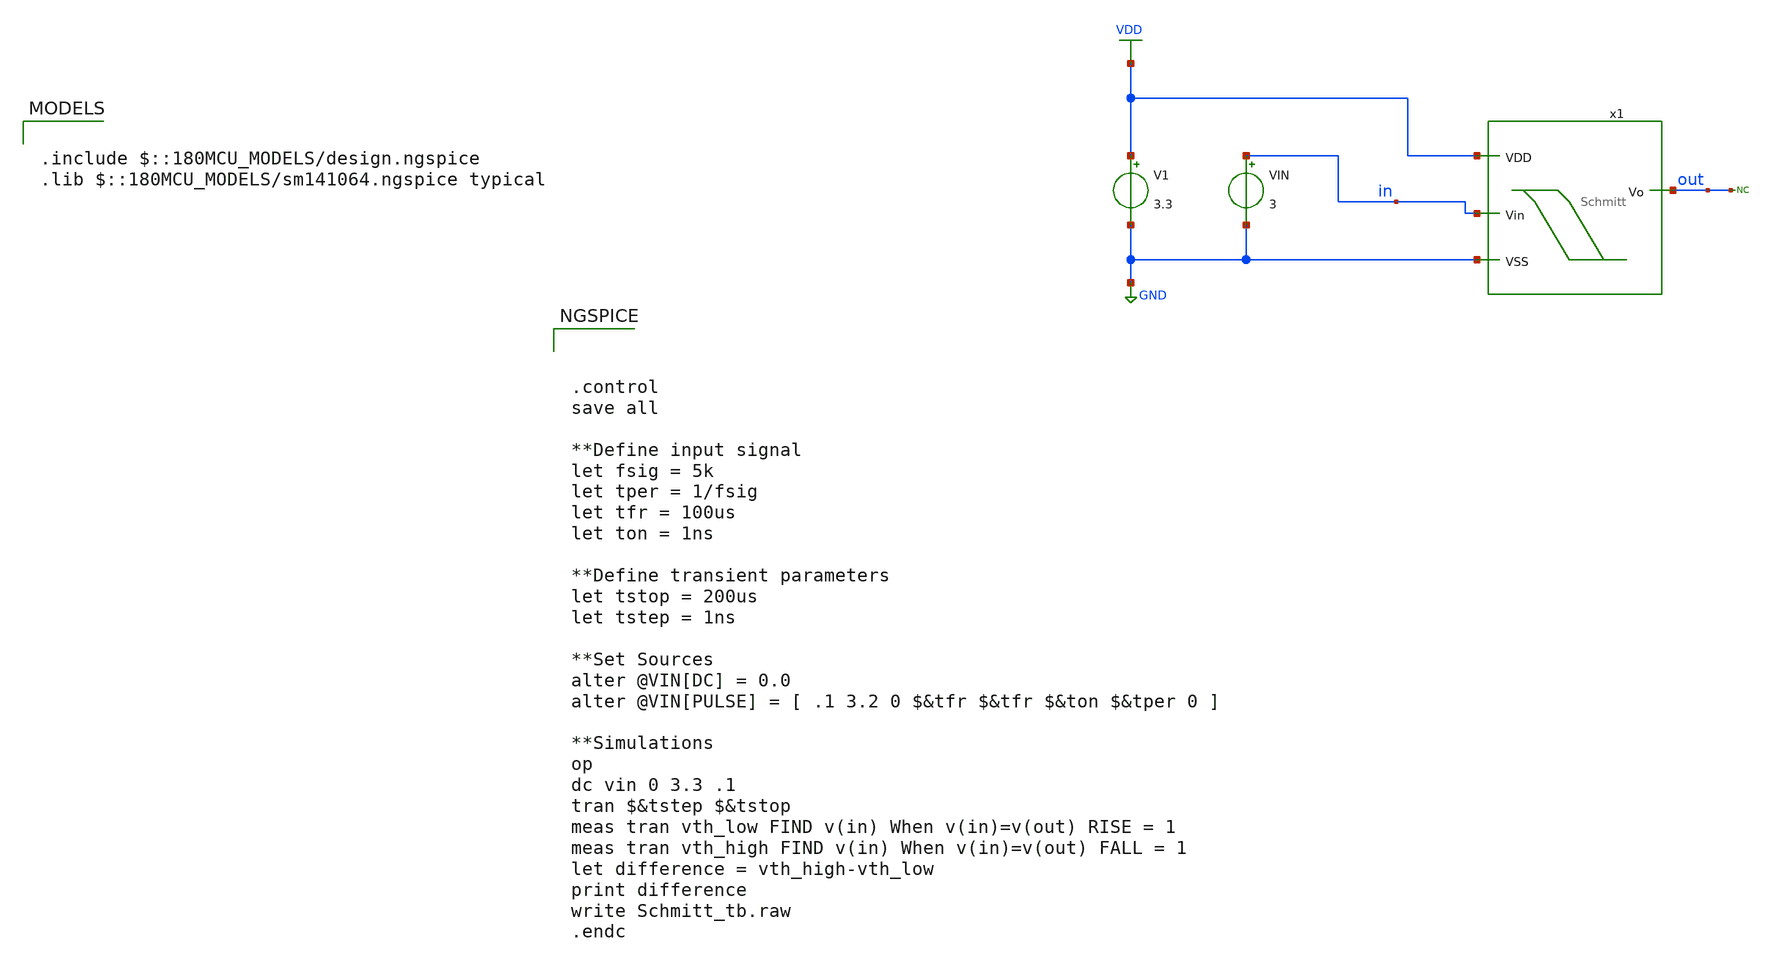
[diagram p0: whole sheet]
** sch_path: designs/switch_matrix_gf180mcu_9t5v0-main/designs/Schmitt_tb.sch
**.subckt Schmitt_tb
x1 VDD in out GND Schmitt
V1 VDD GND 3.3
VIN in GND 3
* noconn out
**** begin user architecture code



.control
save all

**Define input signal
let fsig = 5k
let tper = 1/fsig
let tfr = 100us
let ton = 1ns

**Define transient parameters
let tstop = 200us
let tstep = 1ns

**Set Sources
alter @VIN[DC] = 0.0
alter @VIN[PULSE] = [ .1 3.2 0 $&tfr $&tfr $&ton $&tper 0 ]

**Simulations
op
dc vin 0 3.3 .1
tran $&tstep $&tstop
meas tran vth_low FIND v(in) When v(in)=v(out) RISE = 1
meas tran vth_high FIND v(in) When v(in)=v(out) FALL = 1
let difference = vth_high-vth_low
print difference
write Schmitt_tb.raw
.endc



.include $::180MCU_MODELS/design.ngspice
.lib $::180MCU_MODELS/sm141064.ngspice typical

**** end user architecture code
**.ends

* expanding   symbol:  Schmitt.sym # of pins=4
** sym_path: designs/switch_matrix_gf180mcu_9t5v0-main/designs/Schmitt.sym
** sch_path: designs/switch_matrix_gf180mcu_9t5v0-main/designs/Schmitt.sch
.subckt Schmitt VDD Vin Vo VSS
*.ipin VDD
*.ipin VSS
*.ipin Vin
*.opin Vo
XM2 net2 Vin net3 VSS nfet_03v3 L=0.28u W=2u nf=1 ad='int((nf+1)/2) * W/nf * 0.18u' as='int((nf+2)/2) * W/nf * 0.18u'
+ pd='2*int((nf+1)/2) * (W/nf + 0.18u)' ps='2*int((nf+2)/2) * (W/nf + 0.18u)' nrd='0.18u / W' nrs='0.18u / W'
+ sa=0 sb=0 sd=0 m=1
XM4 net1 Vin VDD VDD pfet_03v3 L=0.28u W=6u nf=1 ad='int((nf+1)/2) * W/nf * 0.18u' as='int((nf+2)/2) * W/nf * 0.18u'
+ pd='2*int((nf+1)/2) * (W/nf + 0.18u)' ps='2*int((nf+2)/2) * (W/nf + 0.18u)' nrd='0.18u / W' nrs='0.18u / W'
+ sa=0 sb=0 sd=0 m=1
XM5 net2 Vin net1 VDD pfet_03v3 L=0.28u W=6u nf=1 ad='int((nf+1)/2) * W/nf * 0.18u' as='int((nf+2)/2) * W/nf * 0.18u'
+ pd='2*int((nf+1)/2) * (W/nf + 0.18u)' ps='2*int((nf+2)/2) * (W/nf + 0.18u)' nrd='0.18u / W' nrs='0.18u / W'
+ sa=0 sb=0 sd=0 m=1
XM1 net3 Vin VSS VSS nfet_03v3 L=0.28u W=2u nf=1 ad='int((nf+1)/2) * W/nf * 0.18u' as='int((nf+2)/2) * W/nf * 0.18u'
+ pd='2*int((nf+1)/2) * (W/nf + 0.18u)' ps='2*int((nf+2)/2) * (W/nf + 0.18u)' nrd='0.18u / W' nrs='0.18u / W'
+ sa=0 sb=0 sd=0 m=1
XM3 VDD net2 net3 VSS nfet_03v3 L=0.28u W=2u nf=1 ad='int((nf+1)/2) * W/nf * 0.18u' as='int((nf+2)/2) * W/nf * 0.18u'
+ pd='2*int((nf+1)/2) * (W/nf + 0.18u)' ps='2*int((nf+2)/2) * (W/nf + 0.18u)' nrd='0.18u / W' nrs='0.18u / W'
+ sa=0 sb=0 sd=0 m=1
XM6 VSS net2 net1 VDD pfet_03v3 L=0.28u W=2u nf=1 ad='int((nf+1)/2) * W/nf * 0.18u' as='int((nf+2)/2) * W/nf * 0.18u'
+ pd='2*int((nf+1)/2) * (W/nf + 0.18u)' ps='2*int((nf+2)/2) * (W/nf + 0.18u)' nrd='0.18u / W' nrs='0.18u / W'
+ sa=0 sb=0 sd=0 m=1
XM7 Vo net2 VSS VSS nfet_03v3 L=0.28u W=2u nf=1 ad='int((nf+1)/2) * W/nf * 0.18u' as='int((nf+2)/2) * W/nf * 0.18u'
+ pd='2*int((nf+1)/2) * (W/nf + 0.18u)' ps='2*int((nf+2)/2) * (W/nf + 0.18u)' nrd='0.18u / W' nrs='0.18u / W'
+ sa=0 sb=0 sd=0 m=1
XM8 Vo net2 VDD VDD pfet_03v3 L=0.28u W=6u nf=1 ad='int((nf+1)/2) * W/nf * 0.18u' as='int((nf+2)/2) * W/nf * 0.18u'
+ pd='2*int((nf+1)/2) * (W/nf + 0.18u)' ps='2*int((nf+2)/2) * (W/nf + 0.18u)' nrd='0.18u / W' nrs='0.18u / W'
+ sa=0 sb=0 sd=0 m=1
.ends

.GLOBAL GND
.GLOBAL VDD
.end
